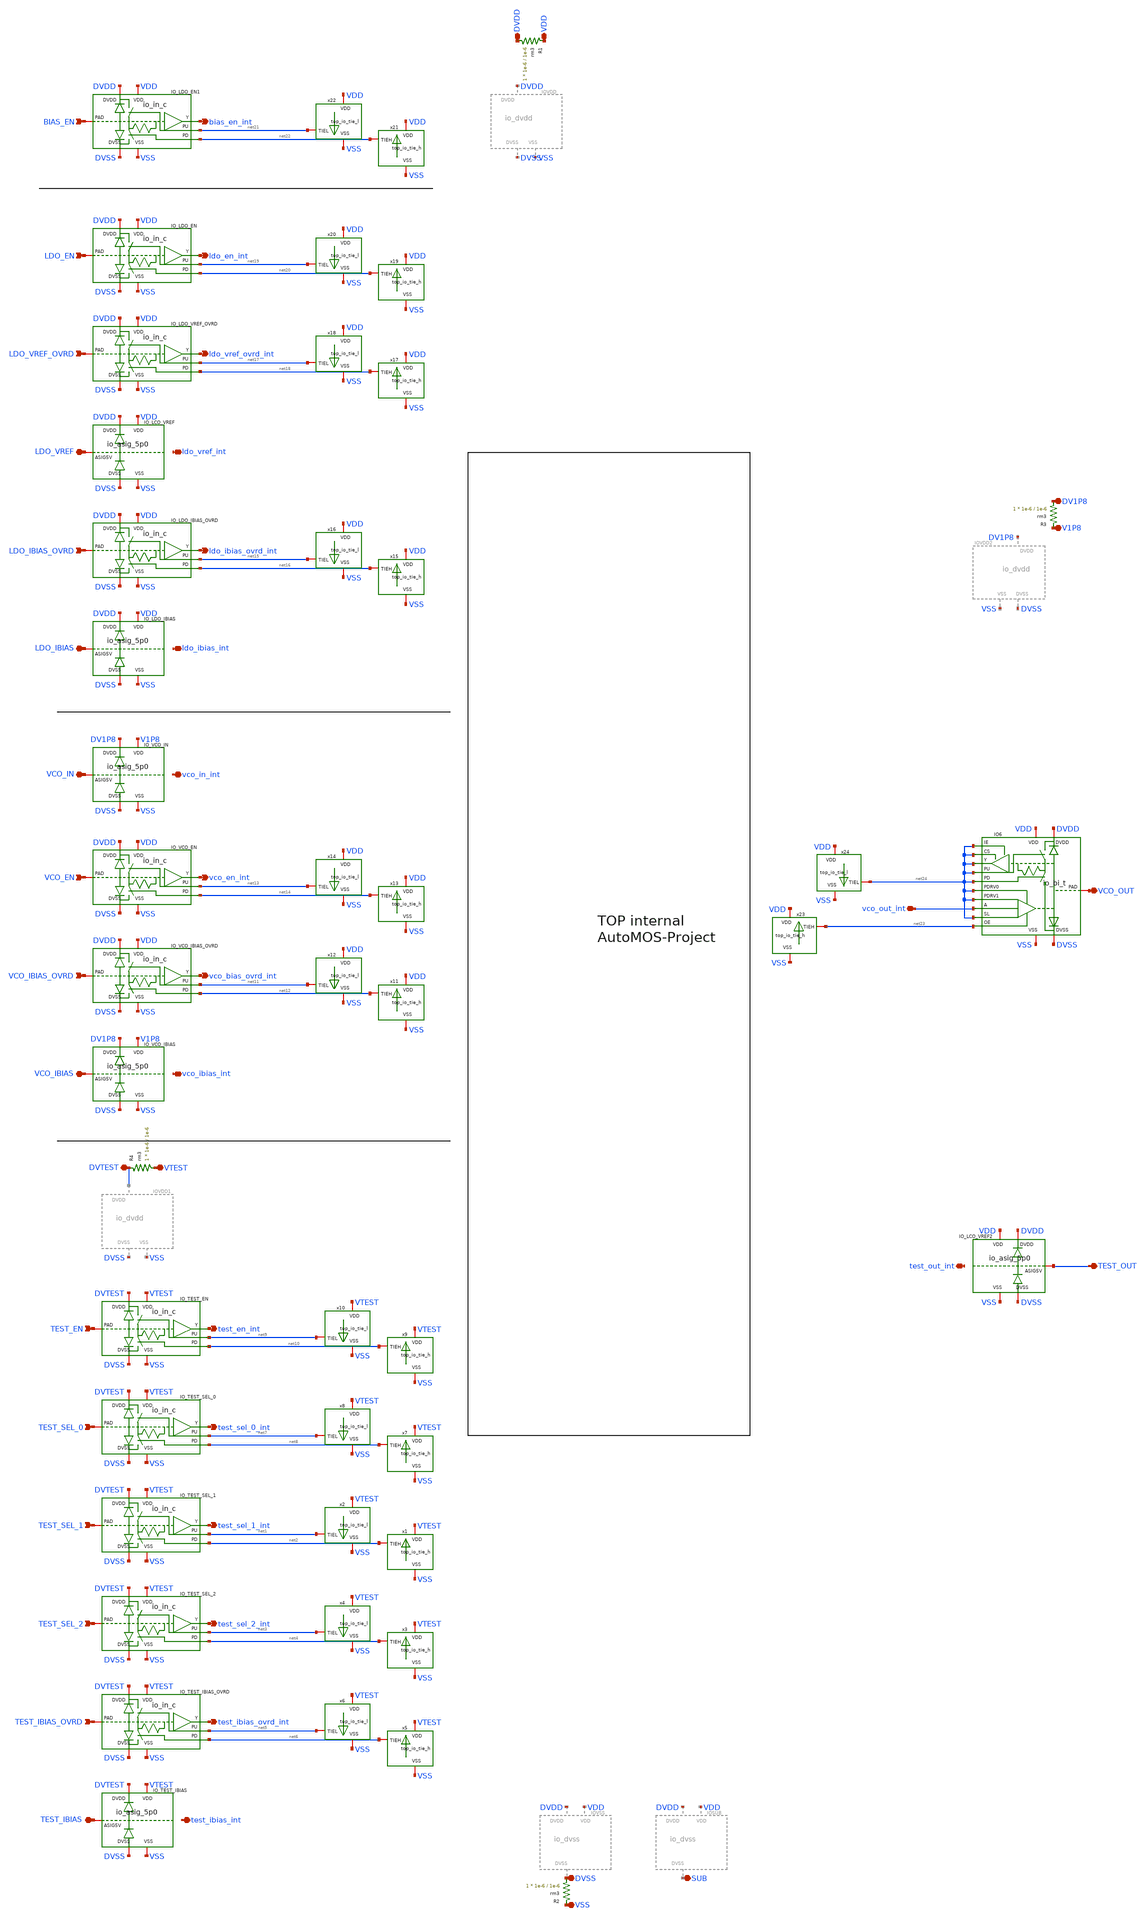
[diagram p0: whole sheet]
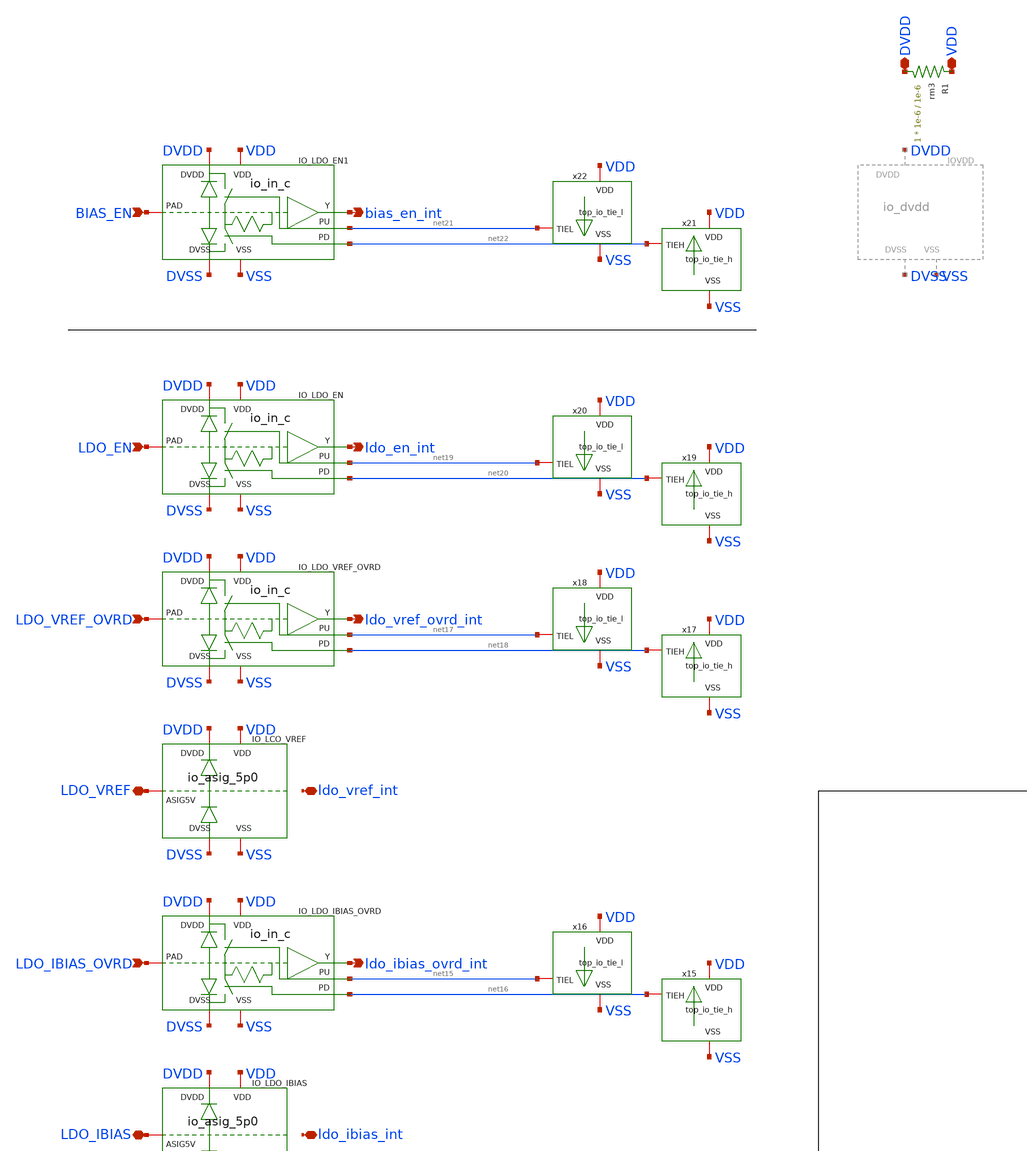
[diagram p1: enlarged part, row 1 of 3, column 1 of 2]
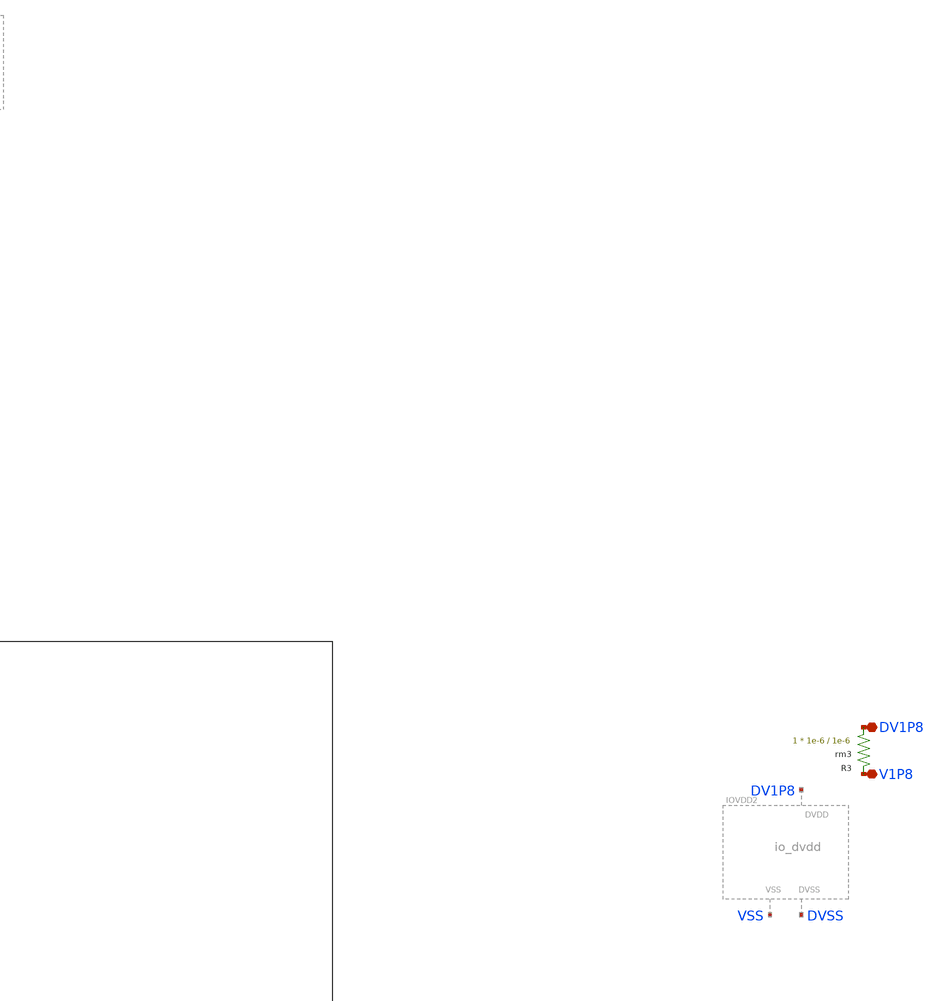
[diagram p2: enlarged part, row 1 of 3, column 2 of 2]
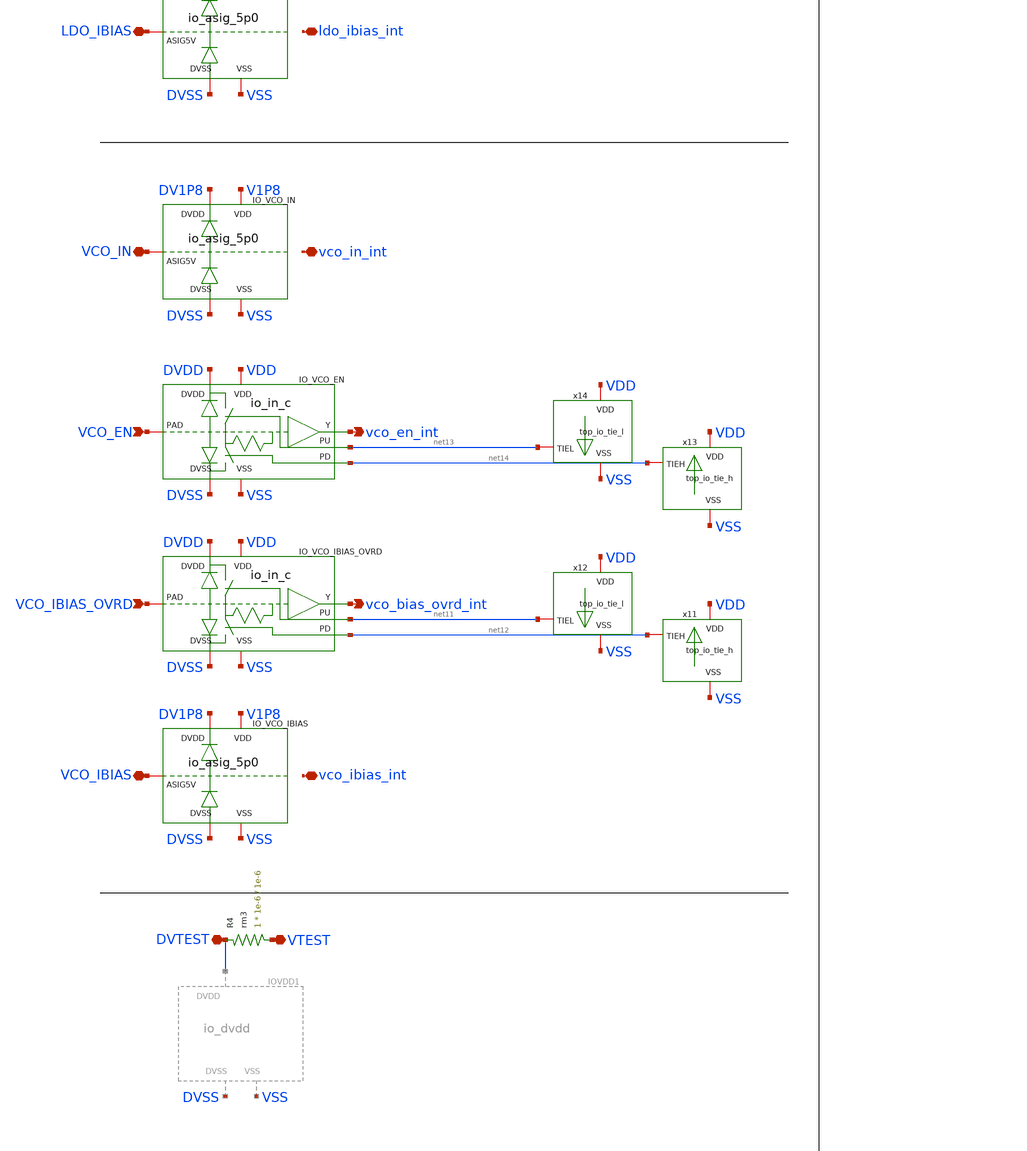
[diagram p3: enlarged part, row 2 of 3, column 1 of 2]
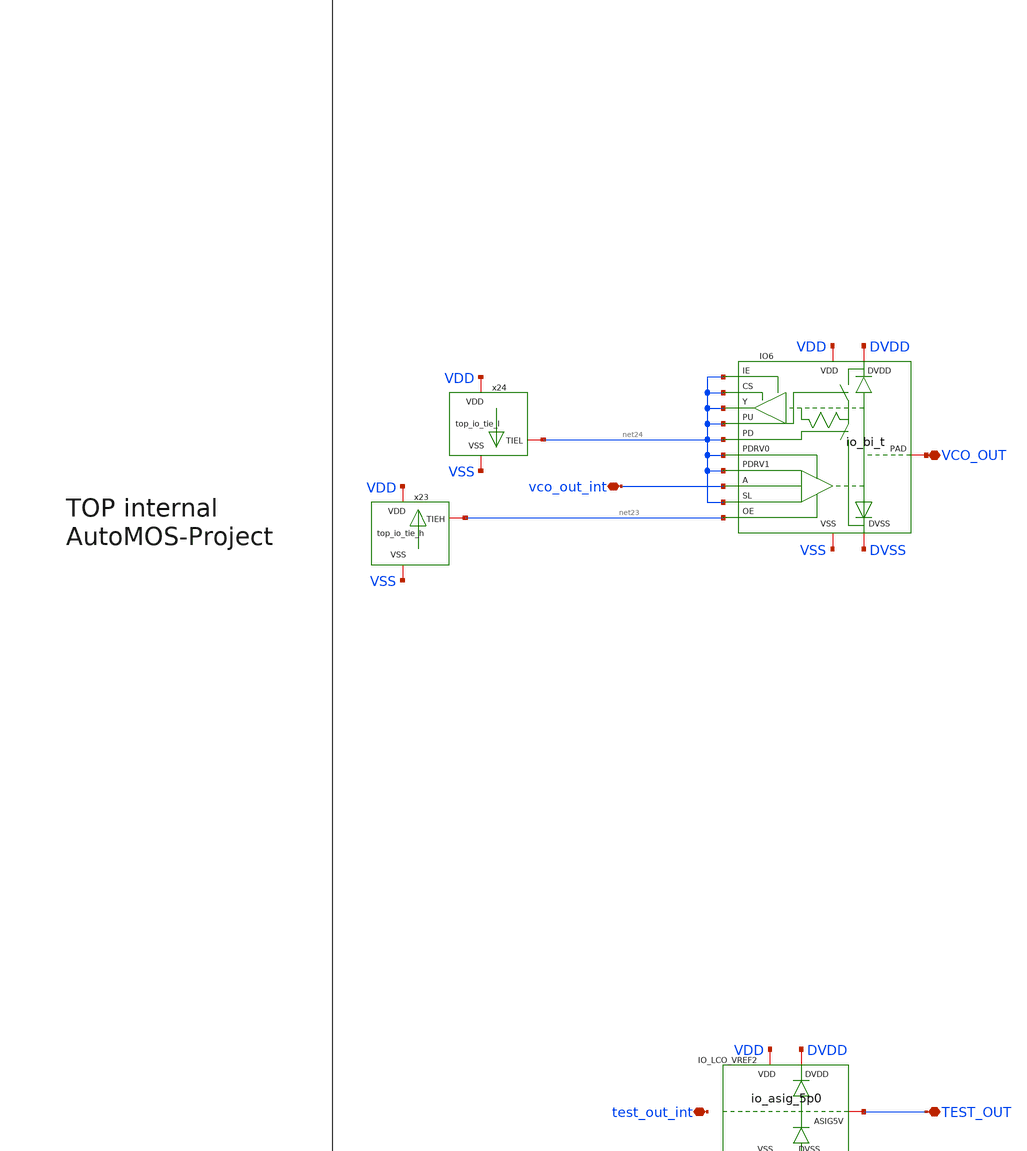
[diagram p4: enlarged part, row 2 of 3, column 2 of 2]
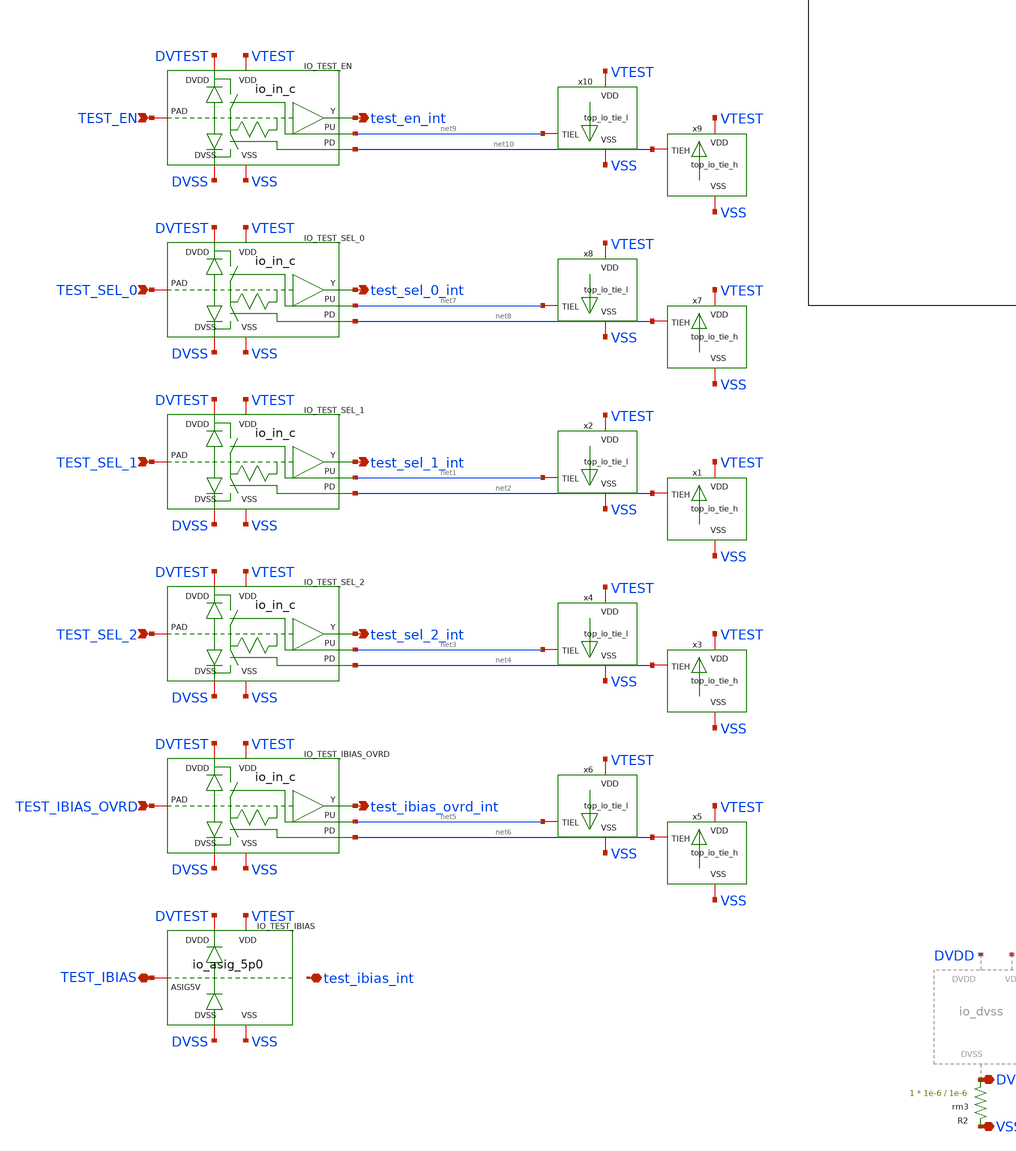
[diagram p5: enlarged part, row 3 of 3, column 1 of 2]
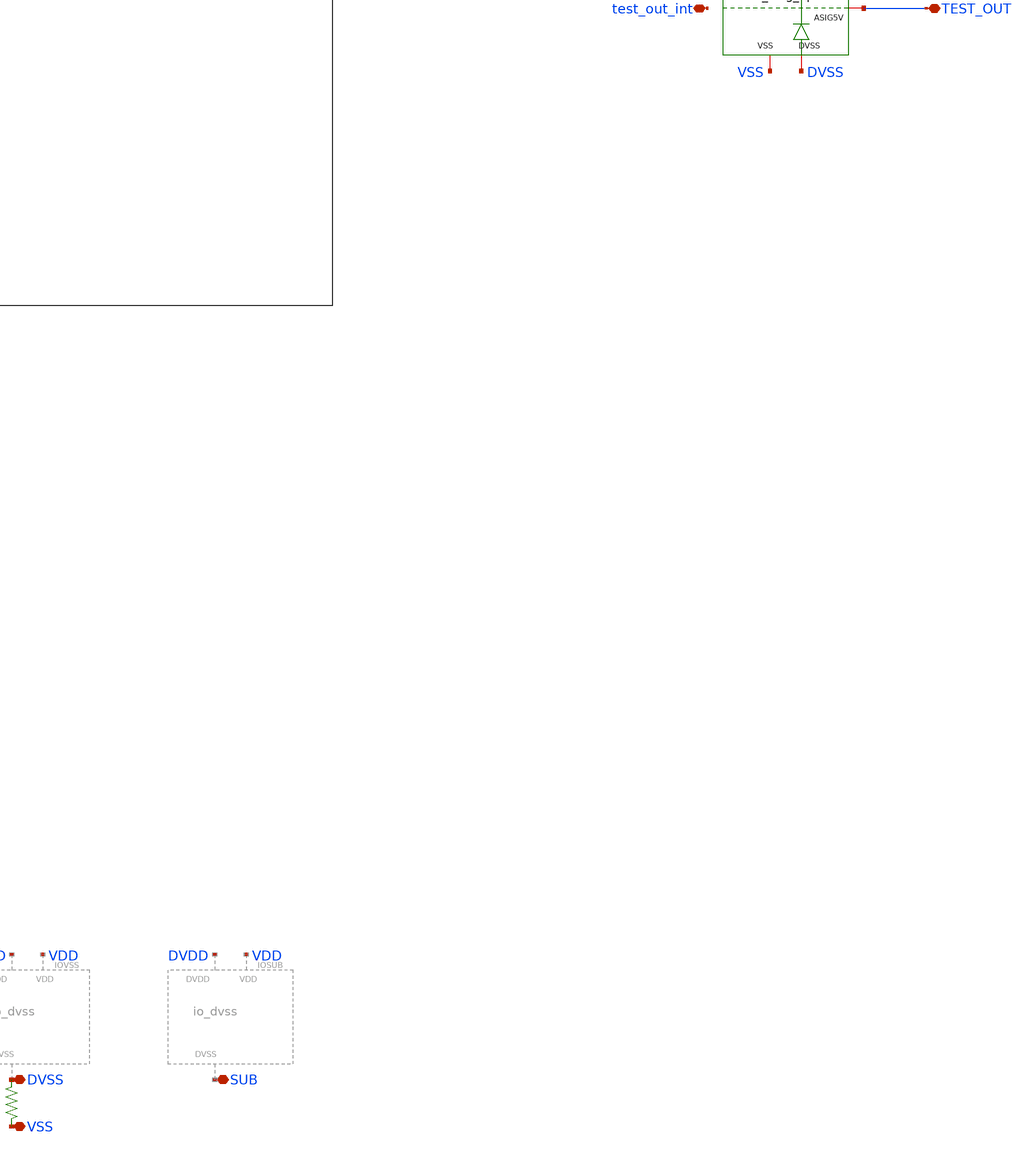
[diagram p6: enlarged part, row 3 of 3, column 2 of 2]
** sch_path: designs/libs/A1_core/top_io/top_io.sch
**.subckt top_io TEST_SEL_0 TEST_SEL_1 TEST_SEL_2 LDO_VREF LDO_IBIAS TEST_IBIAS LDO_VREF_OVRD
*+ LDO_IBIAS_OVRD TEST_IBIAS_OVRD TEST_EN BIAS_EN LDO_EN VDD SUB DVTEST DV1P8 VCO_OUT TEST_OUT VCO_IBIAS
*+ VCO_IBIAS_OVRD VCO_EN VCO_IN test_en_int test_sel_0_int test_sel_1_int test_sel_2_int test_ibias_ovrd_int
*+ test_ibias_int vco_bias_ovrd_int vco_en_int vco_in_int ldo_ibias_ovrd_int ldo_vref_ovrd_int ldo_en_int
*+ ldo_vref_int ldo_ibias_int bias_en_int DVDD DVSS V1P8 test_out_int vco_out_int VTEST VSS vco_ibias_int
*.ipin TEST_SEL_0
*.ipin TEST_SEL_1
*.ipin TEST_SEL_2
*.iopin LDO_VREF
*.iopin LDO_IBIAS
*.iopin TEST_IBIAS
*.ipin LDO_VREF_OVRD
*.ipin LDO_IBIAS_OVRD
*.ipin TEST_IBIAS_OVRD
*.ipin TEST_EN
*.ipin BIAS_EN
*.ipin LDO_EN
*.iopin VDD
*.iopin SUB
*.iopin DVTEST
*.iopin DV1P8
*.iopin VCO_OUT
*.iopin TEST_OUT
*.iopin VCO_IBIAS
*.ipin VCO_IBIAS_OVRD
*.ipin VCO_EN
*.iopin VCO_IN
*.opin test_en_int
*.opin test_sel_0_int
*.opin test_sel_1_int
*.opin test_sel_2_int
*.opin test_ibias_ovrd_int
*.iopin test_ibias_int
*.opin vco_bias_ovrd_int
*.opin vco_en_int
*.iopin vco_in_int
*.opin ldo_ibias_ovrd_int
*.opin ldo_vref_ovrd_int
*.opin ldo_en_int
*.iopin ldo_vref_int
*.iopin ldo_ibias_int
*.opin bias_en_int
*.iopin DVDD
*.iopin DVSS
*.iopin V1P8
*.iopin test_out_int
*.iopin vco_out_int
*.iopin VTEST
*.iopin VSS
*.iopin vco_ibias_int
XIO_TEST_IBIAS TEST_IBIAS DVTEST DVSS VTEST VSS gf180mcu_fd_io__asig_5p0_extracted
XIO_TEST_IBIAS_OVRD DVTEST DVSS TEST_IBIAS_OVRD net6 net5 VTEST VSS test_ibias_ovrd_int
+ gf180mcu_fd_io__in_c
XIO6 vco_out_int net24 DVDD DVSS net24 net23 VCO_OUT net24 net24 net24 net24 net24 VDD VSS net24
+ gf180mcu_fd_io__bi_t
XIO_TEST_SEL_2 DVTEST DVSS TEST_SEL_2 net4 net3 VTEST VSS test_sel_2_int gf180mcu_fd_io__in_c
XIO_TEST_SEL_1 DVTEST DVSS TEST_SEL_1 net2 net1 VTEST VSS test_sel_1_int gf180mcu_fd_io__in_c
XIO_TEST_SEL_0 DVTEST DVSS TEST_SEL_0 net8 net7 VTEST VSS test_sel_0_int gf180mcu_fd_io__in_c
XIO_VCO_IBIAS VCO_IBIAS DV1P8 DVSS V1P8 VSS gf180mcu_fd_io__asig_5p0_extracted
XIO_VCO_IBIAS_OVRD DVDD DVSS VCO_IBIAS_OVRD net12 net11 VDD VSS vco_bias_ovrd_int
+ gf180mcu_fd_io__in_c
XIO_VCO_EN DVDD DVSS VCO_EN net14 net13 VDD VSS vco_en_int gf180mcu_fd_io__in_c
XIO_VCO_IN VCO_IN DV1P8 DVSS V1P8 VSS gf180mcu_fd_io__asig_5p0_extracted
XIO_LDO_IBIAS LDO_IBIAS DVDD DVSS VDD VSS gf180mcu_fd_io__asig_5p0_extracted
XIO_LDO_IBIAS_OVRD DVDD DVSS LDO_IBIAS_OVRD net16 net15 VDD VSS ldo_ibias_ovrd_int
+ gf180mcu_fd_io__in_c
XIO_LCO_VREF LDO_VREF DVDD DVSS VDD VSS gf180mcu_fd_io__asig_5p0_extracted
XIO_LDO_VREF_OVRD DVDD DVSS LDO_VREF_OVRD net18 net17 VDD VSS ldo_vref_ovrd_int gf180mcu_fd_io__in_c
XIO_LDO_EN DVDD DVSS LDO_EN net20 net19 VDD VSS ldo_en_int gf180mcu_fd_io__in_c
XIO_TEST_EN DVTEST DVSS TEST_EN net10 net9 VTEST VSS test_en_int gf180mcu_fd_io__in_c
XIO_LCO_VREF2 TEST_OUT DVDD DVSS VDD VSS gf180mcu_fd_io__asig_5p0_extracted
x1 VTEST net2 VSS top_io_tie_h
x2 VTEST net1 VSS top_io_tie_l
x3 VTEST net4 VSS top_io_tie_h
x4 VTEST net3 VSS top_io_tie_l
x5 VTEST net6 VSS top_io_tie_h
x6 VTEST net5 VSS top_io_tie_l
x7 VTEST net8 VSS top_io_tie_h
x8 VTEST net7 VSS top_io_tie_l
x9 VTEST net10 VSS top_io_tie_h
x10 VTEST net9 VSS top_io_tie_l
x11 VDD net12 VSS top_io_tie_h
x12 VDD net11 VSS top_io_tie_l
x13 VDD net14 VSS top_io_tie_h
x14 VDD net13 VSS top_io_tie_l
x15 VDD net16 VSS top_io_tie_h
x16 VDD net15 VSS top_io_tie_l
x17 VDD net18 VSS top_io_tie_h
x18 VDD net17 VSS top_io_tie_l
x19 VDD net20 VSS top_io_tie_h
x20 VDD net19 VSS top_io_tie_l
XIO_LDO_EN1 DVDD DVSS BIAS_EN net22 net21 VDD VSS bias_en_int gf180mcu_fd_io__in_c
x21 VDD net22 VSS top_io_tie_h
x22 VDD net21 VSS top_io_tie_l
x23 VDD net23 VSS top_io_tie_h
x24 VDD net24 VSS top_io_tie_l
XR1 DVDD VDD rm3 r_width=1e-6 r_length=1e-6 m=1
XR2 DVSS VSS rm3 r_width=1e-6 r_length=1e-6 m=1
XR3 DV1P8 V1P8 rm3 r_width=1e-6 r_length=1e-6 m=1
XR4 VTEST DVTEST rm3 r_width=1e-6 r_length=1e-6 m=1
**.ends
.end
